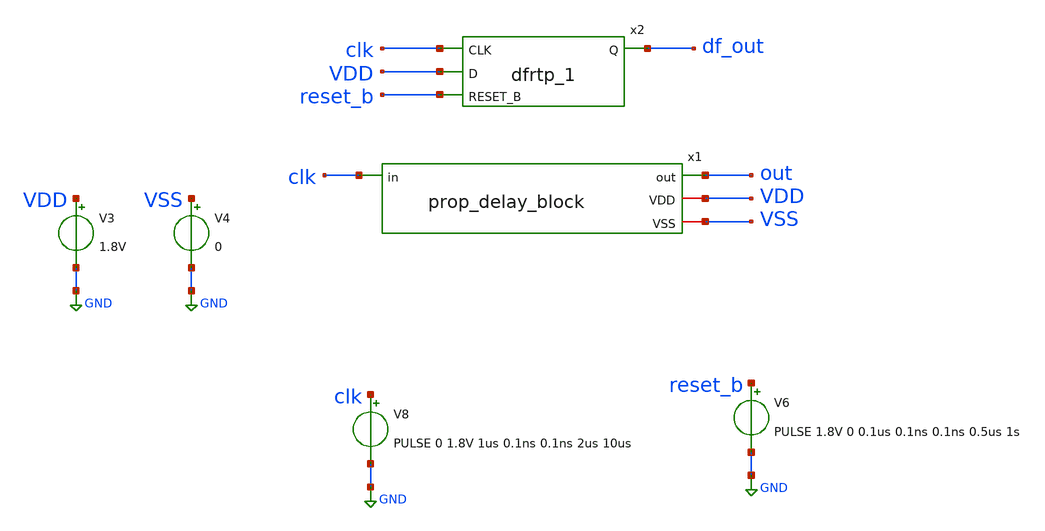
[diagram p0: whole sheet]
** sch_path: xschem/tests/prop_delay_block/prop_delay_block.sch
**.subckt prop_delay_block
V3 VDD GND 1.8V
V4 VSS GND 0
x1 clk out VDD VSS prop_delay_block
V8 clk GND PULSE 0 1.8V 1us 0.1ns 0.1ns 2us 10us
x2 clk VDD reset_b VSS VSS VDD VDD df_out sky130_fd_sc_hd__dfrtp_1
V6 reset_b GND PULSE 1.8V 0 0.1us 0.1ns 0.1ns 0.5us 1s
**** begin user architecture code
 .lib $::SKYWATER_MODELS/sky130.lib.spice tt
.include $::SKYWATER_STDCELLS/sky130_fd_sc_hd.spice


.options acct list
.temp 25
*vvcc VDD 0 dc 1.8
*vvss VSS 0 0
.control
tran 0.1n 2u
plot reset_b-2 clk df_out+2 out+4
write prop_delay_block.raw
.endc


**** end user architecture code
**.ends

* expanding   symbol:  src/prop_delay_block/prop_delay_block.sym # of pins=4
** sym_path: xschem/src/prop_delay_block/prop_delay_block.sym
** sch_path: xschem/src/prop_delay_block/prop_delay_block.sch
.subckt prop_delay_block in out VDD VSS
*.ipin in
*.opin out
*.iopin VDD
*.iopin VSS
x1 in VSS VSS VDD VDD net1 sky130_fd_sc_hd__clkdlybuf4s50_1
x2 net1 VSS VSS VDD VDD out sky130_fd_sc_hd__buf_1
.ends

.GLOBAL GND
.end
